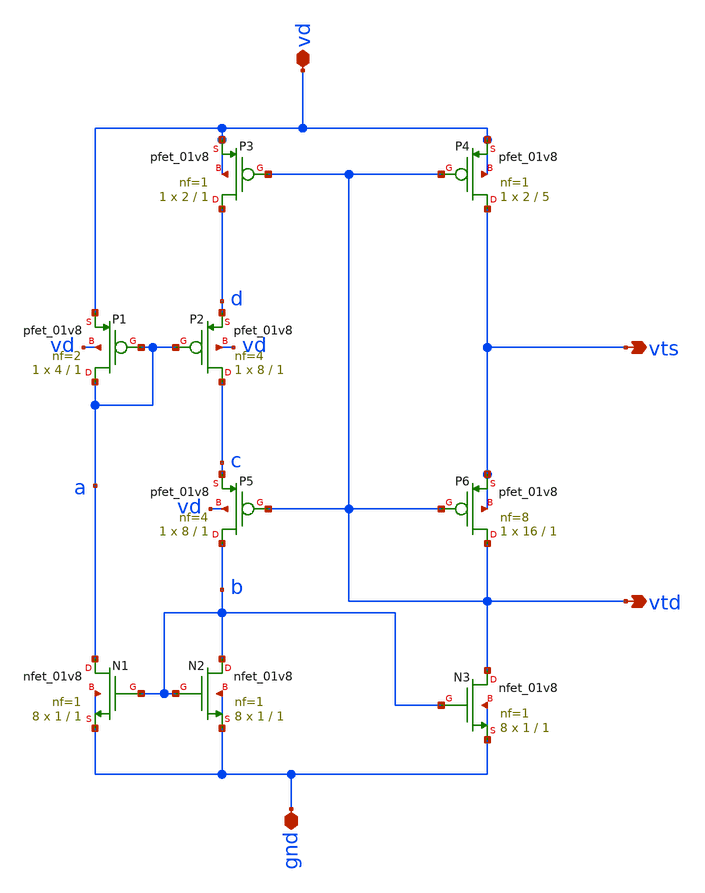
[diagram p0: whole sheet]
** sch_path: mag/sensor/xschem/sensor-no-dummies.sch
**.subckt sensor-no-dummies vd vts vtd gnd
*.iopin vd
*.opin vts
*.opin vtd
*.iopin gnd
XP1 a a vd vd sky130_fd_pr__pfet_01v8 L=1 W=4 nf=2 ad='int((nf+1)/2) * W/nf * 0.29' as='int((nf+2)/2) * W/nf * 0.29'
+ pd='2*int((nf+1)/2) * (W/nf + 0.29)' ps='2*int((nf+2)/2) * (W/nf + 0.29)' nrd='0.29 / W' nrs='0.29 / W'
+ sa=0 sb=0 sd=0 mult=1 m=1
XP2 c a d vd sky130_fd_pr__pfet_01v8 L=1 W=8 nf=4 ad='int((nf+1)/2) * W/nf * 0.29' as='int((nf+2)/2) * W/nf * 0.29'
+ pd='2*int((nf+1)/2) * (W/nf + 0.29)' ps='2*int((nf+2)/2) * (W/nf + 0.29)' nrd='0.29 / W' nrs='0.29 / W'
+ sa=0 sb=0 sd=0 mult=1 m=1
XP3 d vtd vd vd sky130_fd_pr__pfet_01v8 L=1 W=2 nf=1 ad='int((nf+1)/2) * W/nf * 0.29' as='int((nf+2)/2) * W/nf * 0.29'
+ pd='2*int((nf+1)/2) * (W/nf + 0.29)' ps='2*int((nf+2)/2) * (W/nf + 0.29)' nrd='0.29 / W' nrs='0.29 / W'
+ sa=0 sb=0 sd=0 mult=1 m=1
XP4 vts vtd vd vd sky130_fd_pr__pfet_01v8 L=5 W=2 nf=1 ad='int((nf+1)/2) * W/nf * 0.29' as='int((nf+2)/2) * W/nf * 0.29'
+ pd='2*int((nf+1)/2) * (W/nf + 0.29)' ps='2*int((nf+2)/2) * (W/nf + 0.29)' nrd='0.29 / W' nrs='0.29 / W'
+ sa=0 sb=0 sd=0 mult=1 m=1
XP5 b vtd c vd sky130_fd_pr__pfet_01v8 L=1 W=8 nf=4 ad='int((nf+1)/2) * W/nf * 0.29' as='int((nf+2)/2) * W/nf * 0.29'
+ pd='2*int((nf+1)/2) * (W/nf + 0.29)' ps='2*int((nf+2)/2) * (W/nf + 0.29)' nrd='0.29 / W' nrs='0.29 / W'
+ sa=0 sb=0 sd=0 mult=1 m=1
XP6 vtd vtd vts vts sky130_fd_pr__pfet_01v8 L=1 W=16 nf=8 ad='int((nf+1)/2) * W/nf * 0.29' as='int((nf+2)/2) * W/nf * 0.29'
+ pd='2*int((nf+1)/2) * (W/nf + 0.29)' ps='2*int((nf+2)/2) * (W/nf + 0.29)' nrd='0.29 / W' nrs='0.29 / W'
+ sa=0 sb=0 sd=0 mult=1 m=1
XN1 a b gnd gnd sky130_fd_pr__nfet_01v8 L=1 W=1 nf=1 ad='int((nf+1)/2) * W/nf * 0.29' as='int((nf+2)/2) * W/nf * 0.29'
+ pd='2*int((nf+1)/2) * (W/nf + 0.29)' ps='2*int((nf+2)/2) * (W/nf + 0.29)' nrd='0.29 / W' nrs='0.29 / W'
+ sa=0 sb=0 sd=0 mult=8 m=8
XN2 b b gnd gnd sky130_fd_pr__nfet_01v8 L=1 W=1 nf=1 ad='int((nf+1)/2) * W/nf * 0.29' as='int((nf+2)/2) * W/nf * 0.29'
+ pd='2*int((nf+1)/2) * (W/nf + 0.29)' ps='2*int((nf+2)/2) * (W/nf + 0.29)' nrd='0.29 / W' nrs='0.29 / W'
+ sa=0 sb=0 sd=0 mult=8 m=8
XN3 vtd b gnd gnd sky130_fd_pr__nfet_01v8 L=1 W=1 nf=1 ad='int((nf+1)/2) * W/nf * 0.29' as='int((nf+2)/2) * W/nf * 0.29'
+ pd='2*int((nf+1)/2) * (W/nf + 0.29)' ps='2*int((nf+2)/2) * (W/nf + 0.29)' nrd='0.29 / W' nrs='0.29 / W'
+ sa=0 sb=0 sd=0 mult=8 m=8
**.ends
.end
